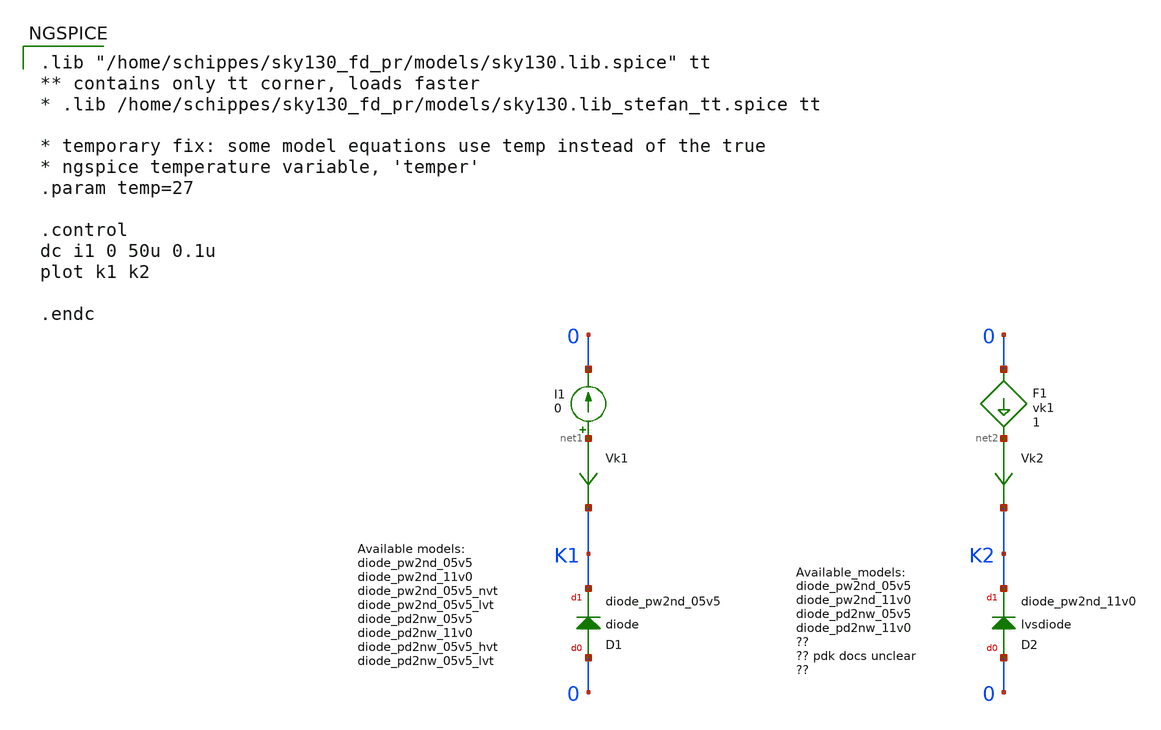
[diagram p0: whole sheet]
** sch_path: sky130_tests/test_diode.sch
**.subckt test_diode
I1 net1 0 0
Vk1 net1 K1 0
.save i(vk1)
D1 0 K1 sky130_fd_pr__diode_pw2nd_05v5 area=1
Vk2 net2 K2 0
.save i(vk2)
D2 0 K2 sky130_fd_pr__diode_pw2nd_11v0 area=1
F1 0 net2 vk1 1
**** begin user architecture code

.lib "/home/schippes/sky130_fd_pr/models/sky130.lib.spice" tt
** contains only tt corner, loads faster
* .lib /home/schippes/sky130_fd_pr/models/sky130.lib_stefan_tt.spice tt

* temporary fix: some model equations use temp instead of the true
* ngspice temperature variable, 'temper'
.param temp=27

.control
dc i1 0 50u 0.1u
plot k1 k2

.endc


**** end user architecture code
**.ends
.end
